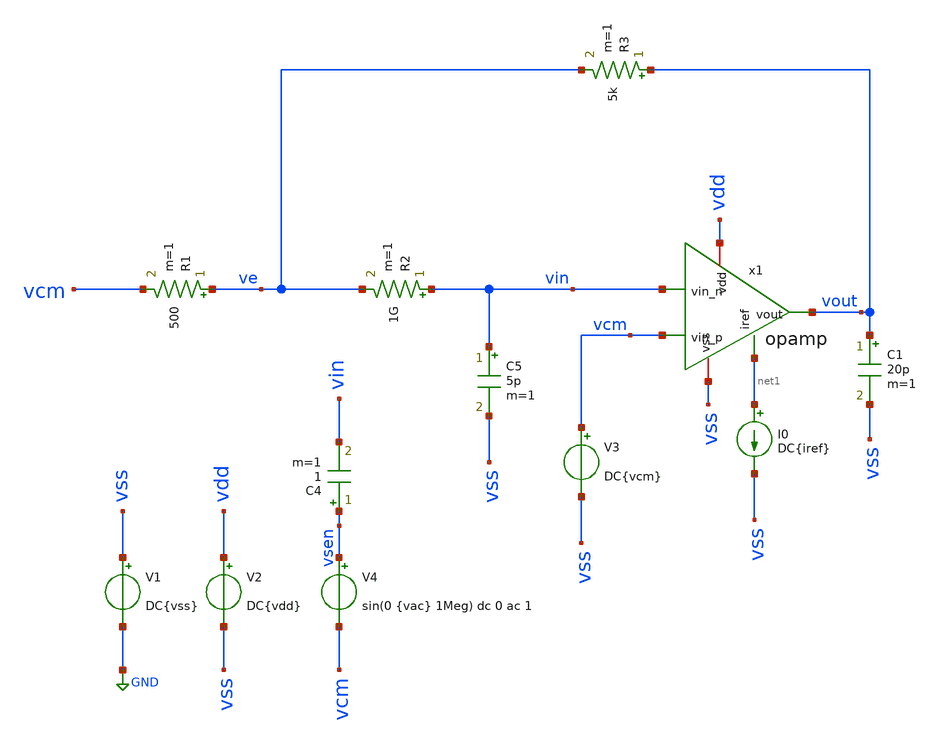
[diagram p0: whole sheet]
** sch_path: sch/opamp/opamp_openloop.sch
**.subckt opamp_openloop
V1 vss GND DC{vss}
V2 vdd vss DC{vdd}
V3 vcm vss DC{vcm}
V4 vsen vcm sin(0 {vac} 1Meg) dc 0 ac 1
C4 vsen vin 1 m=1
I0 net1 vss DC{iref}
R1 ve vcm 500 m=1
R2 vin ve 1G m=1
R3 vout ve 5k m=1
C5 vin vss 5p m=1
C1 vout vss 20p m=1
x1 vdd net1 vin vcm vout vss opamp
**.ends

* expanding   symbol:  opamp/opamp.sym # of pins=6
** sym_path: sch/opamp/opamp.sym
** sch_path: sch/opamp/opamp.sch
.subckt opamp vdd iref vin_n vin_p vout vss
*.iopin vdd
*.iopin vss
*.ipin vin_n
*.ipin vin_p
*.ipin iref
*.opin vout
XM1 vbn vin_n vp vp sky130_fd_pr__pfet_01v8 L=0.3 W=3 nf=1 ad='W * 0.29' as='W * 0.29' pd='2 * (W + 0.29)'
+ ps='2 * (W + 0.29)' nrd='0.29 / W' nrs='0.29 / W' sa=0 sb=0 sd=0 mult=200 m=200
XM2 voe1 vin_p vp vp sky130_fd_pr__pfet_01v8 L=0.3 W=3 nf=1 ad='W * 0.29' as='W * 0.29' pd='2 * (W + 0.29)'
+ ps='2 * (W + 0.29)' nrd='0.29 / W' nrs='0.29 / W' sa=0 sb=0 sd=0 mult=200 m=200
XM3 vbn vbn vss vss sky130_fd_pr__nfet_01v8 L=0.3 W=3 nf=1 ad='W * 0.29' as='W * 0.29' pd='2 * (W + 0.29)'
+ ps='2 * (W + 0.29)' nrd='0.29 / W' nrs='0.29 / W' sa=0 sb=0 sd=0 mult=30 m=30
XM4 voe1 vbn vss vss sky130_fd_pr__nfet_01v8 L=0.3 W=3 nf=1 ad='W * 0.29' as='W * 0.29' pd='2 * (W + 0.29)'
+ ps='2 * (W + 0.29)' nrd='0.29 / W' nrs='0.29 / W' sa=0 sb=0 sd=0 mult=30 m=30
XM5 vp iref vdd vdd sky130_fd_pr__pfet_01v8 L=0.3 W=3 nf=1 ad='W * 0.29' as='W * 0.29' pd='2 * (W + 0.29)'
+ ps='2 * (W + 0.29)' nrd='0.29 / W' nrs='0.29 / W' sa=0 sb=0 sd=0 mult=30 m=30
XM7 vout iref vdd vdd sky130_fd_pr__pfet_01v8 L=0.3 W=3 nf=1 ad='W * 0.29' as='W * 0.29' pd='2 * (W + 0.29)'
+ ps='2 * (W + 0.29)' nrd='0.29 / W' nrs='0.29 / W' sa=0 sb=0 sd=0 mult=150 m=150
XM8 iref iref vdd vdd sky130_fd_pr__pfet_01v8 L=0.3 W=3 nf=1 ad='W * 0.29' as='W * 0.29' pd='2 * (W + 0.29)'
+ ps='2 * (W + 0.29)' nrd='0.29 / W' nrs='0.29 / W' sa=0 sb=0 sd=0 mult=15 m=15
XM9 net1 vdd voe1 vss sky130_fd_pr__nfet_01v8 L=0.15 W=0.75 nf=1 ad='W * 0.29' as='W * 0.29' pd='2 * (W + 0.29)'
+ ps='2 * (W + 0.29)' nrd='0.29 / W' nrs='0.29 / W' sa=0 sb=0 sd=0 mult=6 m=6
XC1 net1 vout sky130_fd_pr__cap_mim_m3_1 W=17.55 L=15 MF=6 m=6
XM6 vout voe1 vss vss sky130_fd_pr__nfet_01v8 L=0.45 W=4.5 nf=1 ad='W * 0.29' as='W * 0.29' pd='2 * (W + 0.29)'
+ ps='2 * (W + 0.29)' nrd='0.29 / W' nrs='0.29 / W' sa=0 sb=0 sd=0 mult=150 m=150
.ends

.GLOBAL GND
.end
